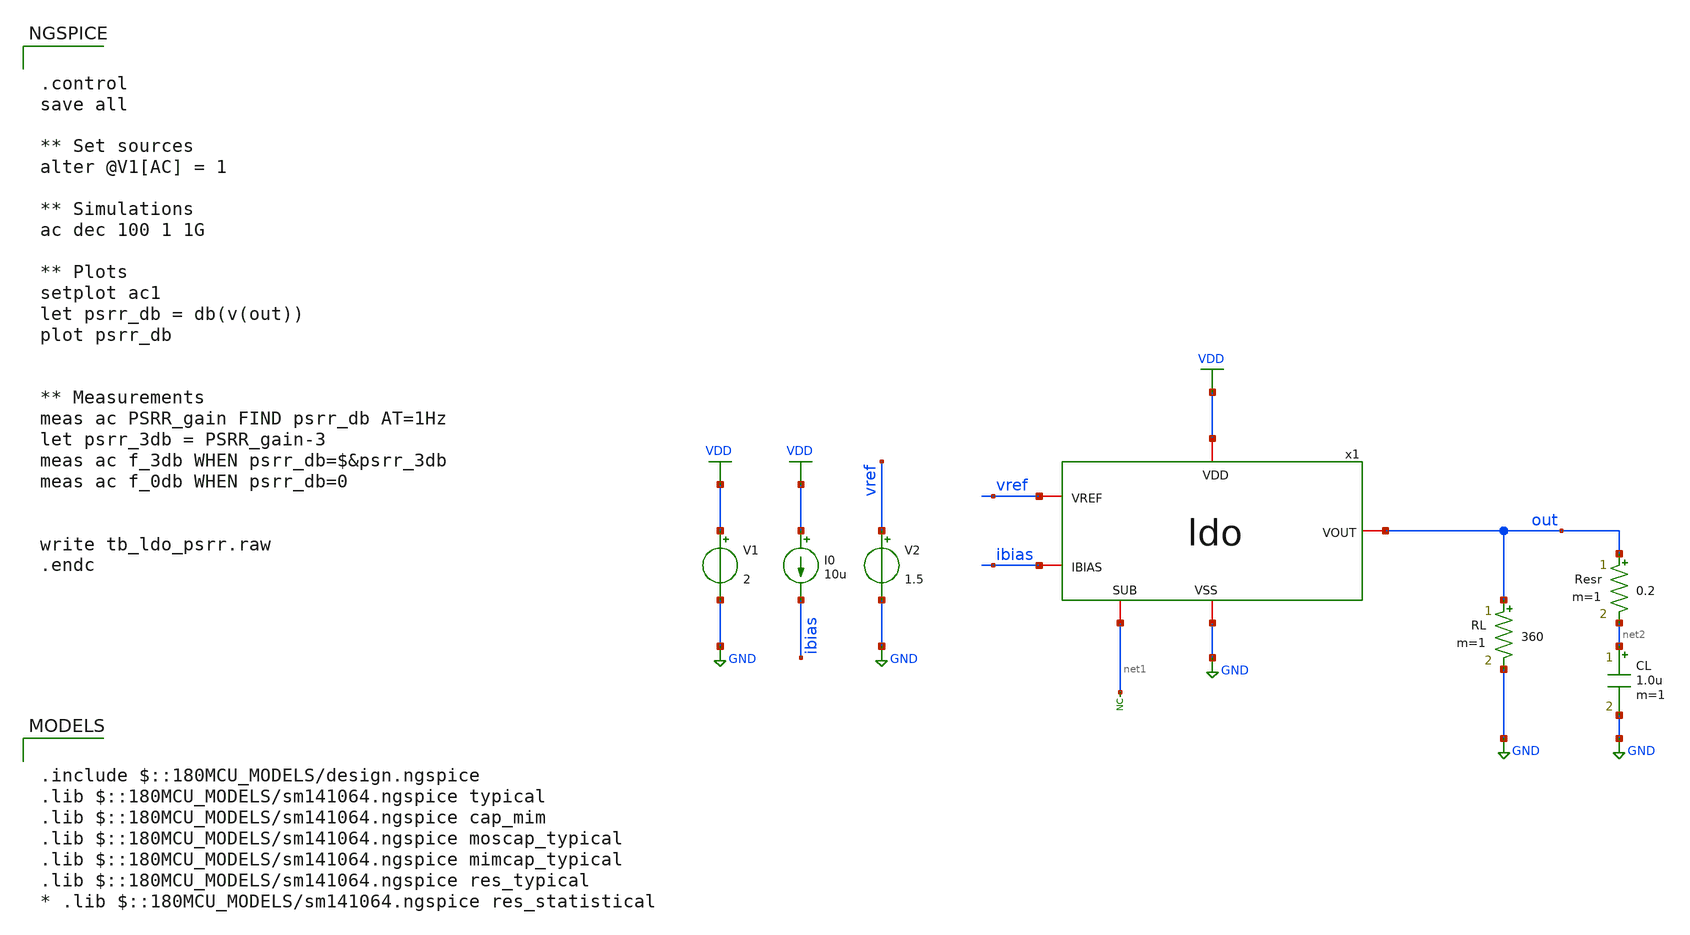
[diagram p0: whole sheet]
** sch_path: designs/libs/tb_ldo/tb_ldo/tb_ldo/tb_ldo_psrr/tb_ldo_psrr.sch
**.subckt tb_ldo_psrr
* noconn #net1
RL out GND 360 m=1
V1 VDD GND 2
V2 vref GND 1.5
I0 VDD ibias 10u
CL net2 GND 1.0u m=1
Resr out net2 0.2 m=1
x1 VDD vref out ibias net1 GND ldo
**** begin user architecture code

.include $::180MCU_MODELS/design.ngspice
.lib $::180MCU_MODELS/sm141064.ngspice typical
.lib $::180MCU_MODELS/sm141064.ngspice cap_mim
.lib $::180MCU_MODELS/sm141064.ngspice moscap_typical
.lib $::180MCU_MODELS/sm141064.ngspice mimcap_typical
.lib $::180MCU_MODELS/sm141064.ngspice res_typical
* .lib $::180MCU_MODELS/sm141064.ngspice res_statistical



.control
save all

** Set sources
alter @V1[AC] = 1

** Simulations
ac dec 100 1 1G

** Plots
setplot ac1
let psrr_db = db(v(out))
plot psrr_db


** Measurements
meas ac PSRR_gain FIND psrr_db AT=1Hz
let psrr_3db = PSRR_gain-3
meas ac f_3db WHEN psrr_db=$&psrr_3db
meas ac f_0db WHEN psrr_db=0


write tb_ldo_psrr.raw
.endc


**** end user architecture code
**.ends

* expanding   symbol:  libs/core_ldo/ldo/ldo/ldo.sym # of pins=6
** sym_path: designs/libs/core_ldo/ldo/ldo/ldo.sym
** sch_path: designs/libs/core_ldo/ldo/ldo/ldo.sch
.subckt ldo VDD VREF VOUT IBIAS SUB VSS
*.iopin VDD
*.iopin VSS
*.iopin VOUT
*.iopin SUB
*.iopin VREF
*.iopin IBIAS
XMp VOUT Vota VDD VDD pfet_05v0 L=0.50u W=100.00u nf=1 ad='int((nf+1)/2) * W/nf * 0.18u' as='int((nf+2)/2) * W/nf * 0.18u'
+ pd='2*int((nf+1)/2) * (W/nf + 0.18u)' ps='2*int((nf+2)/2) * (W/nf + 0.18u)' nrd='0.18u / W' nrs='0.18u / W'
+ sa=0 sb=0 sd=0 m=5
* noconn SUB
x1 VDD VREF net1 Vota IBIAS VSS OTA
XR1 net1 VOUT VDD ppolyf_u_1k r_width=1e-6 r_length=10e-6 m=1
XR2 VSS net1 VDD ppolyf_u_1k r_width=1e-6 r_length=50e-6 m=1
XRc VOUT net2 VDD ppolyf_u_1k r_width=1e-6 r_length=5e-6 m=1
XCc Vota net2 cap_mim_1f0fF c_width=10e-6 c_length=10e-6 m=10
.ends


* expanding   symbol:  libs/core_ldo/ldo/ldo_OTA/OTA.sym # of pins=6
** sym_path: designs/libs/core_ldo/ldo/OTA.sym
** sch_path: designs/libs/core_ldo/ldo/OTA.sch
.subckt OTA VDD VREF VFB VOTA IBIAS VSS
*.iopin VDD
*.iopin VSS
*.iopin VOTA
*.iopin VREF
*.iopin IBIAS
*.iopin VFB
XM3 net2 net2 VDD VDD pfet_05v0 L=2.00u W=8.00u nf=1 ad='int((nf+1)/2) * W/nf * 0.18u' as='int((nf+2)/2) * W/nf * 0.18u'
+ pd='2*int((nf+1)/2) * (W/nf + 0.18u)' ps='2*int((nf+2)/2) * (W/nf + 0.18u)' nrd='0.18u / W' nrs='0.18u / W'
+ sa=0 sb=0 sd=0 m=1
XM4 net3 net3 VDD VDD pfet_05v0 L=2.00u W=8.00u nf=1 ad='int((nf+1)/2) * W/nf * 0.18u' as='int((nf+2)/2) * W/nf * 0.18u'
+ pd='2*int((nf+1)/2) * (W/nf + 0.18u)' ps='2*int((nf+2)/2) * (W/nf + 0.18u)' nrd='0.18u / W' nrs='0.18u / W'
+ sa=0 sb=0 sd=0 m=1
XM5 net4 net2 VDD VDD pfet_05v0 L=2.00u W=8.00u nf=1 ad='int((nf+1)/2) * W/nf * 0.18u' as='int((nf+2)/2) * W/nf * 0.18u'
+ pd='2*int((nf+1)/2) * (W/nf + 0.18u)' ps='2*int((nf+2)/2) * (W/nf + 0.18u)' nrd='0.18u / W' nrs='0.18u / W'
+ sa=0 sb=0 sd=0 m=1
XM6 VOTA net3 VDD VDD pfet_05v0 L=2.00u W=8.00u nf=1 ad='int((nf+1)/2) * W/nf * 0.18u' as='int((nf+2)/2) * W/nf * 0.18u'
+ pd='2*int((nf+1)/2) * (W/nf + 0.18u)' ps='2*int((nf+2)/2) * (W/nf + 0.18u)' nrd='0.18u / W' nrs='0.18u / W'
+ sa=0 sb=0 sd=0 m=2
XM9 IBIAS IBIAS VSS VSS nfet_05v0 L=2.00u W=4.00u nf=1 ad='int((nf+1)/2) * W/nf * 0.18u' as='int((nf+2)/2) * W/nf * 0.18u'
+ pd='2*int((nf+1)/2) * (W/nf + 0.18u)' ps='2*int((nf+2)/2) * (W/nf + 0.18u)' nrd='0.18u / W' nrs='0.18u / W'
+ sa=0 sb=0 sd=0 m=1
XM10 net1 IBIAS VSS VSS nfet_05v0 L=2.00u W=4.00u nf=1 ad='int((nf+1)/2) * W/nf * 0.18u' as='int((nf+2)/2) * W/nf * 0.18u'
+ pd='2*int((nf+1)/2) * (W/nf + 0.18u)' ps='2*int((nf+2)/2) * (W/nf + 0.18u)' nrd='0.18u / W' nrs='0.18u / W'
+ sa=0 sb=0 sd=0 m=1
XM7 net4 net4 VSS VSS nfet_05v0 L=2.00u W=4.00u nf=1 ad='int((nf+1)/2) * W/nf * 0.18u' as='int((nf+2)/2) * W/nf * 0.18u'
+ pd='2*int((nf+1)/2) * (W/nf + 0.18u)' ps='2*int((nf+2)/2) * (W/nf + 0.18u)' nrd='0.18u / W' nrs='0.18u / W'
+ sa=0 sb=0 sd=0 m=1
XM8 VOTA net4 VSS VSS nfet_05v0 L=2.00u W=4.00u nf=1 ad='int((nf+1)/2) * W/nf * 0.18u' as='int((nf+2)/2) * W/nf * 0.18u'
+ pd='2*int((nf+1)/2) * (W/nf + 0.18u)' ps='2*int((nf+2)/2) * (W/nf + 0.18u)' nrd='0.18u / W' nrs='0.18u / W'
+ sa=0 sb=0 sd=0 m=2
XM1 net2 VREF net1 net1 nfet_05v0 L=0.60u W=40.00u nf=1 ad='int((nf+1)/2) * W/nf * 0.18u' as='int((nf+2)/2) * W/nf * 0.18u'
+ pd='2*int((nf+1)/2) * (W/nf + 0.18u)' ps='2*int((nf+2)/2) * (W/nf + 0.18u)' nrd='0.18u / W' nrs='0.18u / W'
+ sa=0 sb=0 sd=0 m=1
XM2 net3 VFB net1 net1 nfet_05v0 L=0.60u W=40.00u nf=1 ad='int((nf+1)/2) * W/nf * 0.18u' as='int((nf+2)/2) * W/nf * 0.18u'
+ pd='2*int((nf+1)/2) * (W/nf + 0.18u)' ps='2*int((nf+2)/2) * (W/nf + 0.18u)' nrd='0.18u / W' nrs='0.18u / W'
+ sa=0 sb=0 sd=0 m=1
.ends

.GLOBAL GND
.GLOBAL VDD
.end
